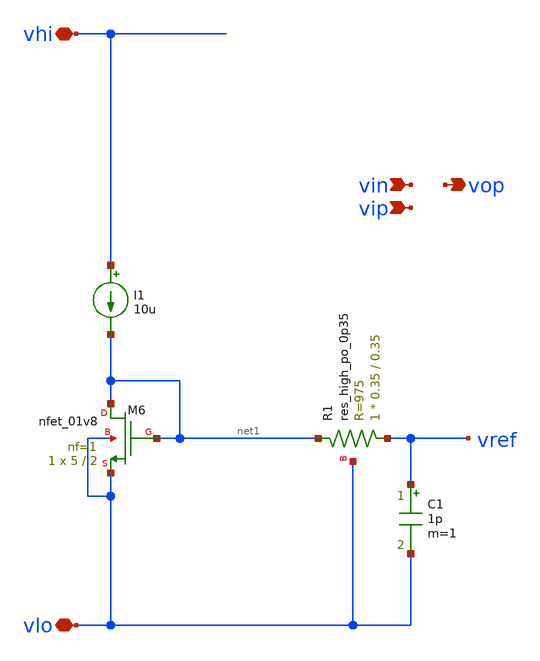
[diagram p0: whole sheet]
** sch_path: xschem/i_type_ota_PEX.sch
**.subckt i_type_ota_PEX vip vin vop vhi vlo
*.ipin vip
*.ipin vin
*.opin vop
*.iopin vhi
*.iopin vlo
XM6 net1 net1 vlo vlo sky130_fd_pr__nfet_01v8 L=2 W=5 nf=1 ad='int((nf+1)/2) * W/nf * 0.29' as='int((nf+2)/2) * W/nf * 0.29'
+ pd='2*int((nf+1)/2) * (W/nf + 0.29)' ps='2*int((nf+2)/2) * (W/nf + 0.29)' nrd='0.29 / W' nrs='0.29 / W'
+ sa=0 sb=0 sd=0 mult=1 m=1
I1 vhi net1 10u
XR1 vref net1 vlo sky130_fd_pr__res_high_po_0p35 L=0.35 mult=1 m=1
C1 vref vlo 1p m=1
**** begin user architecture code

* NGSPICE file created from cmota_1_flat.ext - technology: sky130A

.subckt cmota_1_flat VHI VLO VREF VIP VIN VOP
* NGSPICE file created from cmota_1_flat_1.ext - technology: sky130A
* NGSPICE file created from cmota_1_flat_1.ext - technology: sky130A

X0 VHI a_266_188# a_147_n2312# VHI sky130_fd_pr__pfet_01v8 ad=0p pd=0u as=0p ps=0u w=1e+07u
+ l=300000u
X1 VHI a_266_188# a_147_n2312# VHI sky130_fd_pr__pfet_01v8 ad=0p pd=0u as=0p ps=0u w=1e+07u
+ l=300000u
X2 VHI a_2626_188# VOP VHI sky130_fd_pr__pfet_01v8 ad=0p pd=0u as=0p ps=0u w=1e+07u l=300000u
X3 a_266_188# VIN a_1799_n900# VLO sky130_fd_pr__nfet_01v8_lvt ad=0p pd=0u as=0p ps=0u w=2.5e+06u
+ l=150000u
X4 VHI a_2626_188# VOP VHI sky130_fd_pr__pfet_01v8 ad=0p pd=0u as=0p ps=0u w=1e+07u l=300000u
X5 a_1799_n900# VIN a_266_188# VLO sky130_fd_pr__nfet_01v8_lvt ad=0p pd=0u as=0p ps=0u w=2.5e+06u
+ l=150000u
X6 a_2626_188# VIP a_1799_n900# VLO sky130_fd_pr__nfet_01v8_lvt ad=0p pd=0u as=0p ps=0u w=2.5e+06u
+ l=150000u
X7 a_147_n2312# a_266_188# VHI VHI sky130_fd_pr__pfet_01v8 ad=0p pd=0u as=0p ps=0u w=1e+07u
+ l=300000u
X8 a_147_n2312# a_266_188# VHI VHI sky130_fd_pr__pfet_01v8 ad=0p pd=0u as=0p ps=0u w=1e+07u
+ l=300000u
X9 VHI a_2626_188# VOP VHI sky130_fd_pr__pfet_01v8 ad=0p pd=0u as=0p ps=0u w=1e+07u l=300000u
X10 a_2626_188# a_2626_188# VHI VHI sky130_fd_pr__pfet_01v8 ad=0p pd=0u as=0p ps=0u w=1e+07u
+ l=300000u
X11 a_2626_188# VIP a_1799_n900# VLO sky130_fd_pr__nfet_01v8_lvt ad=0p pd=0u as=0p ps=0u w=2.5e+06u
+ l=150000u
X12 VOP a_2626_188# VHI VHI sky130_fd_pr__pfet_01v8 ad=0p pd=0u as=0p ps=0u w=1e+07u l=300000u
X13 VLO a_147_n2312# a_147_n2312# VLO sky130_fd_pr__nfet_01v8 ad=0p pd=0u as=0p ps=0u w=1e+07u
+ l=300000u
X14 a_147_n2312# a_147_n2312# VLO VLO sky130_fd_pr__nfet_01v8 ad=0p pd=0u as=0p ps=0u w=1e+07u
+ l=300000u
X15 VOP a_2626_188# VHI VHI sky130_fd_pr__pfet_01v8 ad=0p pd=0u as=0p ps=0u w=1e+07u l=300000u
X16 VOP a_2626_188# VHI VHI sky130_fd_pr__pfet_01v8 ad=0p pd=0u as=0p ps=0u w=1e+07u l=300000u
X17 VOP a_2626_188# VHI VHI sky130_fd_pr__pfet_01v8 ad=0p pd=0u as=0p ps=0u w=1e+07u l=300000u
X18 VLO VLO VLO VLO sky130_fd_pr__nfet_01v8 ad=0p pd=0u as=0p ps=0u w=1e+07u l=300000u
X19 a_1799_n900# VLO VLO VLO sky130_fd_pr__nfet_01v8_lvt ad=0p pd=0u as=0p ps=0u w=2.5e+06u
+ l=150000u
X20 VLO a_147_n2312# VOP VLO sky130_fd_pr__nfet_01v8 ad=0p pd=0u as=0p ps=0u w=1e+07u l=300000u
X21 VHI a_266_188# a_147_n2312# VHI sky130_fd_pr__pfet_01v8 ad=0p pd=0u as=0p ps=0u w=1e+07u
+ l=300000u
X22 VOP a_147_n2312# VLO VLO sky130_fd_pr__nfet_01v8 ad=0p pd=0u as=0p ps=0u w=1e+07u l=300000u
X23 VLO a_147_n2312# VOP VLO sky130_fd_pr__nfet_01v8 ad=0p pd=0u as=0p ps=0u w=1e+07u l=300000u
X24 VOP a_147_n2312# VLO VLO sky130_fd_pr__nfet_01v8 ad=0p pd=0u as=0p ps=0u w=1e+07u l=300000u
X25 VHI a_2626_188# a_2626_188# VHI sky130_fd_pr__pfet_01v8 ad=0p pd=0u as=0p ps=0u w=1e+07u
+ l=300000u
X26 VHI a_2626_188# VOP VHI sky130_fd_pr__pfet_01v8 ad=0p pd=0u as=0p ps=0u w=1e+07u l=300000u
X27 a_1799_n900# VIP a_2626_188# VLO sky130_fd_pr__nfet_01v8_lvt ad=0p pd=0u as=0p ps=0u w=2.5e+06u
+ l=150000u
X28 VLO VREF a_1799_n900# VLO sky130_fd_pr__nfet_01v8 ad=0p pd=0u as=0p ps=0u w=1e+07u l=2e+06u
X29 a_147_n2312# a_266_188# VHI VHI sky130_fd_pr__pfet_01v8 ad=0p pd=0u as=0p ps=0u w=1e+07u
+ l=300000u
X30 a_147_n2312# a_266_188# VHI VHI sky130_fd_pr__pfet_01v8 ad=0p pd=0u as=0p ps=0u w=1e+07u
+ l=300000u
X31 VHI a_2626_188# VOP VHI sky130_fd_pr__pfet_01v8 ad=0p pd=0u as=0p ps=0u w=1e+07u l=300000u
X32 VLO VLO VLO VLO sky130_fd_pr__nfet_01v8_lvt ad=0p pd=0u as=0p ps=0u w=2.5e+06u l=150000u
X33 VLO VREF a_1799_n900# VLO sky130_fd_pr__nfet_01v8 ad=0p pd=0u as=0p ps=0u w=1e+07u l=2e+06u
X34 VHI VHI VHI VHI sky130_fd_pr__pfet_01v8 ad=0p pd=0u as=0p ps=0u w=1e+07u l=300000u
X35 VHI VHI VHI VHI sky130_fd_pr__pfet_01v8 ad=0p pd=0u as=0p ps=0u w=1e+07u l=300000u
X36 a_1799_n900# VIN a_266_188# VLO sky130_fd_pr__nfet_01v8_lvt ad=0p pd=0u as=0p ps=0u w=2.5e+06u
+ l=150000u
X37 a_147_n2312# a_266_188# VHI VHI sky130_fd_pr__pfet_01v8 ad=0p pd=0u as=0p ps=0u w=1e+07u
+ l=300000u
X38 a_2626_188# a_2626_188# VHI VHI sky130_fd_pr__pfet_01v8 ad=0p pd=0u as=0p ps=0u w=1e+07u
+ l=300000u
X39 a_266_188# a_266_188# VHI VHI sky130_fd_pr__pfet_01v8 ad=0p pd=0u as=0p ps=0u w=1e+07u l=300000u
X40 VOP a_2626_188# VHI VHI sky130_fd_pr__pfet_01v8 ad=0p pd=0u as=0p ps=0u w=1e+07u l=300000u
X41 a_266_188# VIN a_1799_n900# VLO sky130_fd_pr__nfet_01v8_lvt ad=0p pd=0u as=0p ps=0u w=2.5e+06u
+ l=150000u
X42 VLO a_147_n2312# a_147_n2312# VLO sky130_fd_pr__nfet_01v8 ad=0p pd=0u as=0p ps=0u w=1e+07u
+ l=300000u
X43 a_1799_n900# VIP a_2626_188# VLO sky130_fd_pr__nfet_01v8_lvt ad=0p pd=0u as=0p ps=0u w=2.5e+06u
+ l=150000u
X44 VHI a_266_188# a_147_n2312# VHI sky130_fd_pr__pfet_01v8 ad=0p pd=0u as=0p ps=0u w=1e+07u
+ l=300000u
X45 VHI a_266_188# a_147_n2312# VHI sky130_fd_pr__pfet_01v8 ad=0p pd=0u as=0p ps=0u w=1e+07u
+ l=300000u
X46 VOP a_2626_188# VHI VHI sky130_fd_pr__pfet_01v8 ad=0p pd=0u as=0p ps=0u w=1e+07u l=300000u
X47 VHI VHI VHI VHI sky130_fd_pr__pfet_01v8 ad=0p pd=0u as=0p ps=0u w=1e+07u l=300000u
X48 a_147_n2312# a_147_n2312# VLO VLO sky130_fd_pr__nfet_01v8 ad=0p pd=0u as=0p ps=0u w=1e+07u
+ l=300000u
X49 VLO a_147_n2312# a_147_n2312# VLO sky130_fd_pr__nfet_01v8 ad=0p pd=0u as=0p ps=0u w=1e+07u
+ l=300000u
X50 VLO VLO VLO VLO sky130_fd_pr__nfet_01v8 ad=0p pd=0u as=0p ps=0u w=1e+07u l=300000u
X51 VOP a_147_n2312# VLO VLO sky130_fd_pr__nfet_01v8 ad=0p pd=0u as=0p ps=0u w=1e+07u l=300000u
X52 VLO a_147_n2312# VOP VLO sky130_fd_pr__nfet_01v8 ad=0p pd=0u as=0p ps=0u w=1e+07u l=300000u
X53 VHI a_266_188# a_266_188# VHI sky130_fd_pr__pfet_01v8 ad=0p pd=0u as=0p ps=0u w=1e+07u l=300000u
X54 VLO a_147_n2312# VOP VLO sky130_fd_pr__nfet_01v8 ad=0p pd=0u as=0p ps=0u w=1e+07u l=300000u
X55 VHI a_266_188# a_147_n2312# VHI sky130_fd_pr__pfet_01v8 ad=0p pd=0u as=0p ps=0u w=1e+07u
+ l=300000u
X56 VHI a_266_188# a_147_n2312# VHI sky130_fd_pr__pfet_01v8 ad=0p pd=0u as=0p ps=0u w=1e+07u
+ l=300000u
X57 VLO VLO a_1799_n900# VLO sky130_fd_pr__nfet_01v8_lvt ad=0p pd=0u as=0p ps=0u w=2.5e+06u
+ l=150000u
X58 a_266_188# VIN a_1799_n900# VLO sky130_fd_pr__nfet_01v8_lvt ad=0p pd=0u as=0p ps=0u w=2.5e+06u
+ l=150000u
X59 VHI a_266_188# a_266_188# VHI sky130_fd_pr__pfet_01v8 ad=0p pd=0u as=0p ps=0u w=1e+07u l=300000u
X60 VHI a_2626_188# VOP VHI sky130_fd_pr__pfet_01v8 ad=0p pd=0u as=0p ps=0u w=1e+07u l=300000u
X61 VHI a_2626_188# VOP VHI sky130_fd_pr__pfet_01v8 ad=0p pd=0u as=0p ps=0u w=1e+07u l=300000u
X62 VLO VLO VLO VLO sky130_fd_pr__nfet_01v8 ad=0p pd=0u as=0p ps=0u w=1e+07u l=300000u
X63 a_1799_n900# VREF VLO VLO sky130_fd_pr__nfet_01v8 ad=0p pd=0u as=0p ps=0u w=1e+07u l=2e+06u
X64 a_147_n2312# a_266_188# VHI VHI sky130_fd_pr__pfet_01v8 ad=0p pd=0u as=0p ps=0u w=1e+07u
+ l=300000u
X65 VLO VLO VLO VLO sky130_fd_pr__nfet_01v8_lvt ad=0p pd=0u as=0p ps=0u w=2.5e+06u l=150000u
X66 a_1799_n900# VIN a_266_188# VLO sky130_fd_pr__nfet_01v8_lvt ad=0p pd=0u as=0p ps=0u w=2.5e+06u
+ l=150000u
X67 a_1799_n900# VREF VLO VLO sky130_fd_pr__nfet_01v8 ad=0p pd=0u as=0p ps=0u w=1e+07u l=2e+06u
X68 a_2626_188# VIP a_1799_n900# VLO sky130_fd_pr__nfet_01v8_lvt ad=0p pd=0u as=0p ps=0u w=2.5e+06u
+ l=150000u
X69 a_147_n2312# a_266_188# VHI VHI sky130_fd_pr__pfet_01v8 ad=0p pd=0u as=0p ps=0u w=1e+07u
+ l=300000u
X70 a_1799_n900# VIN a_266_188# VLO sky130_fd_pr__nfet_01v8_lvt ad=0p pd=0u as=0p ps=0u w=2.5e+06u
+ l=150000u
X71 a_147_n2312# a_266_188# VHI VHI sky130_fd_pr__pfet_01v8 ad=0p pd=0u as=0p ps=0u w=1e+07u
+ l=300000u
X72 VOP a_2626_188# VHI VHI sky130_fd_pr__pfet_01v8 ad=0p pd=0u as=0p ps=0u w=1e+07u l=300000u
X73 a_2626_188# VIP a_1799_n900# VLO sky130_fd_pr__nfet_01v8_lvt ad=0p pd=0u as=0p ps=0u w=2.5e+06u
+ l=150000u
X74 VLO VLO VLO VLO sky130_fd_pr__nfet_01v8 ad=0p pd=0u as=0p ps=0u w=1e+07u l=300000u
X75 a_266_188# a_266_188# VHI VHI sky130_fd_pr__pfet_01v8 ad=0p pd=0u as=0p ps=0u w=1e+07u l=300000u
X76 VOP a_2626_188# VHI VHI sky130_fd_pr__pfet_01v8 ad=0p pd=0u as=0p ps=0u w=1e+07u l=300000u
X77 a_147_n2312# a_147_n2312# VLO VLO sky130_fd_pr__nfet_01v8 ad=0p pd=0u as=0p ps=0u w=1e+07u
+ l=300000u
X78 a_1799_n900# VIP a_2626_188# VLO sky130_fd_pr__nfet_01v8_lvt ad=0p pd=0u as=0p ps=0u w=2.5e+06u
+ l=150000u
X79 a_147_n2312# a_147_n2312# VLO VLO sky130_fd_pr__nfet_01v8 ad=0p pd=0u as=0p ps=0u w=1e+07u
+ l=300000u
X80 VLO a_147_n2312# a_147_n2312# VLO sky130_fd_pr__nfet_01v8 ad=0p pd=0u as=0p ps=0u w=1e+07u
+ l=300000u
X81 VOP a_147_n2312# VLO VLO sky130_fd_pr__nfet_01v8 ad=0p pd=0u as=0p ps=0u w=1e+07u l=300000u
X82 a_1799_n900# VIP a_2626_188# VLO sky130_fd_pr__nfet_01v8_lvt ad=0p pd=0u as=0p ps=0u w=2.5e+06u
+ l=150000u
X83 VHI VHI VHI VHI sky130_fd_pr__pfet_01v8 ad=0p pd=0u as=0p ps=0u w=1e+07u l=300000u
X84 VHI a_266_188# a_147_n2312# VHI sky130_fd_pr__pfet_01v8 ad=0p pd=0u as=0p ps=0u w=1e+07u
+ l=300000u
X85 a_266_188# VIN a_1799_n900# VLO sky130_fd_pr__nfet_01v8_lvt ad=0p pd=0u as=0p ps=0u w=2.5e+06u
+ l=150000u
X86 VHI a_2626_188# a_2626_188# VHI sky130_fd_pr__pfet_01v8 ad=0p pd=0u as=0p ps=0u w=1e+07u
+ l=300000u
X87 VHI a_2626_188# VOP VHI sky130_fd_pr__pfet_01v8 ad=0p pd=0u as=0p ps=0u w=1e+07u l=300000u
C0 a_266_188# a_1799_n900# 5.98fF
C1 a_266_188# a_147_n2312# 2.69fF
C2 VHI VOP 34.99fF
C3 VHI a_2626_188# 13.00fF
C4 VHI a_266_188# 13.03fF
C5 a_2626_188# a_1799_n900# 5.97fF
C6 VHI a_147_n2312# 35.91fF
C7 a_1799_n900# VREF 2.35fF
C8 VREF VLO 7.19fF $ **FLOATING
C9 a_1799_n900# VLO 6.10fF $ **FLOATING
C10 VOP VLO 17.35fF $ **FLOATING
C11 a_147_n2312# VLO 22.96fF $ **FLOATING
C12 VHI VLO 46.50fF $ **FLOATING

.ends


XDUT vhi vlo vref vip vin vop cmota_1_flat


**** end user architecture code
**.ends
.end
